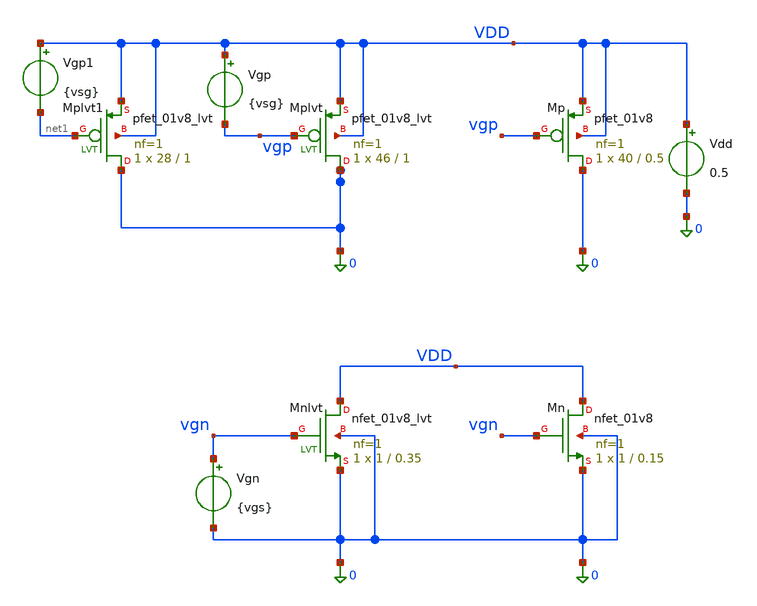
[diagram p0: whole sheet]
** sch_path: xschem/caracterizador.sch
**.subckt caracterizador
Vgp VDD vgp {vsg}
Vdd VDD 0 0.5
XMplvt 0 vgp VDD VDD sky130_fd_pr__pfet_01v8_lvt L=1 W=46 nf=1 ad='int((1 + 1)/2) * 46 / 1 * 0.29' as='int((1 + 2)/2) * 46 / 1 * 0.29'
+ pd='2*int((1 + 1)/2) * (46 / 1 + 0.29)' ps='2*int((1 + 2)/2) * (46 / 1 + 0.29)' nrd='0.29 / 46 ' nrs='0.29 / 46 '
+ sa=0 sb=0 sd=0 mult=1 m=1
XMp 0 vgp VDD VDD sky130_fd_pr__pfet_01v8 L=0.5 W=40 nf=1 ad='int((nf+1)/2) * W/nf * 0.29' as='int((nf+2)/2) * W/nf * 0.29'
+ pd='2*int((nf+1)/2) * (W/nf + 0.29)' ps='2*int((nf+2)/2) * (W/nf + 0.29)' nrd='0.29 / W' nrs='0.29 / W'
+ sa=0 sb=0 sd=0 mult=1 m=1
XMnlvt VDD vgn 0 0 sky130_fd_pr__nfet_01v8_lvt L=0.35 W=1 nf=1 ad='int((1 + 1)/2) * 1 / 1 * 0.29' as='int((1 + 2)/2) * 1 / 1 * 0.29'
+ pd='2*int((1 + 1)/2) * (1 / 1 + 0.29)' ps='2*int((1 + 2)/2) * (1 / 1 + 0.29)' nrd='0.29 / 1 ' nrs='0.29 / 1 '
+ sa=0 sb=0 sd=0 mult=1 m=1
XMn VDD vgn 0 0 sky130_fd_pr__nfet_01v8 L=0.15 W=1 nf=1 ad='int((1 + 1)/2) * 1 / 1 * 0.29' as='int((1 + 2)/2) * 1 / 1 * 0.29'
+ pd='2*int((1 + 1)/2) * (1 / 1 + 0.29)' ps='2*int((1 + 2)/2) * (1 / 1 + 0.29)' nrd='0.29 / 1 ' nrs='0.29 / 1 '
+ sa=0 sb=0 sd=0 mult=1 m=1
Vgn vgn 0 {vgs}
XMplvt1 0 net1 VDD VDD sky130_fd_pr__pfet_01v8_lvt L=1 W=28 nf=1 ad='int((1 + 1)/2) * 28 / 1 * 0.29'
+ as='int((1 + 2)/2) * 28 / 1 * 0.29' pd='2*int((1 + 1)/2) * (28 / 1 + 0.29)' ps='2*int((1 + 2)/2) * (28 / 1 + 0.29)'
+ nrd='0.29 / 28 ' nrs='0.29 / 28 ' sa=0 sb=0 sd=0 mult=1 m=1
Vgp1 VDD net1 {vsg}
**** begin user architecture code


* ==============================================================================
* Encabezado: Caracterizador Completo para PMOS y NMOS Sky130 (Std y LVT)
* Descripcion: Control de simulacion para extraer gm, ro, Id, Vth, Vdsat, Vov,
*              Cgg, ft y gm/Id de los 4 transistores (Mplvt, Mp, Mnlvt, Mn).
* ==============================================================================



* 1. Inclusión de libreria de modelos Sky130 PRIMERO
.lib /foss/pdks/sky130A/libs.tech/ngspice/sky130.lib.spice tt

.option temp=27


* Parametros de tension de polarizacion iniciales
.param vsg = 0.7
.param vgs = 0.6

* Parametros de dimensiones geometricas (en micrometros um)
.param wplvt = 1
.param lplvt = 0.35

.param wp = 1
.param lp = 0.15

.param wnlvt = 1
.param lnlvt = 0.35

.param wn = 1
.param ln = 0.15

.control
  * Forzar comportamiento estandar de SPICE para evitar errores numparam en Sky130
  set ngbehavior=ps

  save all

  * --- 1. GUARDAR PARAMETROS PMOS LVT (xMplvt) ---
  save @m.xMplvt.msky130_fd_pr__pfet_01v8_lvt[gm]
  save @m.xMplvt.msky130_fd_pr__pfet_01v8_lvt[gds]
  save @m.xMplvt.msky130_fd_pr__pfet_01v8_lvt[id]
  save @m.xMplvt.msky130_fd_pr__pfet_01v8_lvt[vth]
  save @m.xMplvt.msky130_fd_pr__pfet_01v8_lvt[vdsat]
  save @m.xMplvt.msky130_fd_pr__pfet_01v8_lvt[cgg]
  save @m.xMplvt.msky130_fd_pr__pfet_01v8_lvt[vgs]

  save @m.xMplvt1.msky130_fd_pr__pfet_01v8_lvt[gm]
  save @m.xMplvt1.msky130_fd_pr__pfet_01v8_lvt[gds]
  save @m.xMplvt1.msky130_fd_pr__pfet_01v8_lvt[id]
  save @m.xMplvt1.msky130_fd_pr__pfet_01v8_lvt[vth]
  save @m.xMplvt1.msky130_fd_pr__pfet_01v8_lvt[vdsat]
  save @m.xMplvt1.msky130_fd_pr__pfet_01v8_lvt[cgg]
  save @m.xMplvt1.msky130_fd_pr__pfet_01v8_lvt[vgs]

  * --- 2. GUARDAR PARAMETROS PMOS ESTANDAR (xMp) ---
  save @m.xMp.msky130_fd_pr__pfet_01v8[gm]
  save @m.xMp.msky130_fd_pr__pfet_01v8[gds]
  save @m.xMp.msky130_fd_pr__pfet_01v8[id]
  save @m.xMp.msky130_fd_pr__pfet_01v8[vth]
  save @m.xMp.msky130_fd_pr__pfet_01v8[vdsat]
  save @m.xMp.msky130_fd_pr__pfet_01v8[cgg]
  save @m.xMp.msky130_fd_pr__pfet_01v8[vgs]

  * --- 3. GUARDAR PARAMETROS NMOS LVT (xMnlvt) ---
  save @m.xMnlvt.msky130_fd_pr__nfet_01v8_lvt[gm]
  save @m.xMnlvt.msky130_fd_pr__nfet_01v8_lvt[gds]
  save @m.xMnlvt.msky130_fd_pr__nfet_01v8_lvt[id]
  save @m.xMnlvt.msky130_fd_pr__nfet_01v8_lvt[vth]
  save @m.xMnlvt.msky130_fd_pr__nfet_01v8_lvt[vdsat]
  save @m.xMnlvt.msky130_fd_pr__nfet_01v8_lvt[cgg]
  save @m.xMnlvt.msky130_fd_pr__nfet_01v8_lvt[vgs]

  * --- 4. GUARDAR PARAMETROS NMOS ESTANDAR (xMn) ---
  save @m.xMn.msky130_fd_pr__nfet_01v8[gm]
  save @m.xMn.msky130_fd_pr__nfet_01v8[gds]
  save @m.xMn.msky130_fd_pr__nfet_01v8[id]
  save @m.xMn.msky130_fd_pr__nfet_01v8[vth]
  save @m.xMn.msky130_fd_pr__nfet_01v8[vdsat]
  save @m.xMn.msky130_fd_pr__nfet_01v8[cgg]
  save @m.xMn.msky130_fd_pr__nfet_01v8[vgs]

  * Barrido DC de fuentes de voltaje Vgp (PMOS) y Vgn (NMOS) de 0V a 1.8V
  dc Vgp 0 1.8 0.01 Vgn 0 1.8 0.01

  * --- CALCULOS PMOS LVT (Mplvt) ---
  let ro_mplvt = 1 / @m.xMplvt.msky130_fd_pr__pfet_01v8_lvt[gds]
  let gm_id_mplvt = @m.xMplvt.msky130_fd_pr__pfet_01v8_lvt[gm] /
+ @m.xMplvt.msky130_fd_pr__pfet_01v8_lvt[id]
  let ft_mplvt = @m.xMplvt.msky130_fd_pr__pfet_01v8_lvt[gm] / (2 * pi *
+ @m.xMplvt.msky130_fd_pr__pfet_01v8_lvt[cgg])
  let vov_mplvt = abs(@m.xMplvt.msky130_fd_pr__pfet_01v8_lvt[vgs]) -
+ abs(@m.xMplvt.msky130_fd_pr__pfet_01v8_lvt[vth])

  * --- CALCULOS PMOS STD (Mp) ---
  let ro_mp = 1 / @m.xMp.msky130_fd_pr__pfet_01v8[gds]
  let gm_id_mp = @m.xMp.msky130_fd_pr__pfet_01v8[gm] / @m.xMp.msky130_fd_pr__pfet_01v8[id]
  let ft_mp = @m.xMp.msky130_fd_pr__pfet_01v8[gm] / (2 * pi * @m.xMp.msky130_fd_pr__pfet_01v8[cgg])
  let vov_mp = abs(@m.xMp.msky130_fd_pr__pfet_01v8[vgs]) - abs(@m.xMp.msky130_fd_pr__pfet_01v8[vth])

  * --- CALCULOS NMOS LVT (Mnlvt) ---
  let ro_mnlvt = 1 / @m.xMnlvt.msky130_fd_pr__nfet_01v8_lvt[gds]
  let gm_id_mnlvt = @m.xMnlvt.msky130_fd_pr__nfet_01v8_lvt[gm] /
+ @m.xMnlvt.msky130_fd_pr__nfet_01v8_lvt[id]
  let ft_mnlvt = @m.xMnlvt.msky130_fd_pr__nfet_01v8_lvt[gm] / (2 * pi *
+ @m.xMnlvt.msky130_fd_pr__nfet_01v8_lvt[cgg])
  let vov_mnlvt = @m.xMnlvt.msky130_fd_pr__nfet_01v8_lvt[vgs] -
+ @m.xMnlvt.msky130_fd_pr__nfet_01v8_lvt[vth]

  * --- CALCULOS NMOS STD (Mn) ---
  let ro_mn = 1 / @m.xMn.msky130_fd_pr__nfet_01v8[gds]
  let gm_id_mn = @m.xMn.msky130_fd_pr__nfet_01v8[gm] / @m.xMn.msky130_fd_pr__nfet_01v8[id]
  let ft_mn = @m.xMn.msky130_fd_pr__nfet_01v8[gm] / (2 * pi * @m.xMn.msky130_fd_pr__nfet_01v8[cgg])
  let vov_mn = @m.xMn.msky130_fd_pr__nfet_01v8[vgs] - @m.xMn.msky130_fd_pr__nfet_01v8[vth]

  * Guardar los resultados en archivo caracterizador.raw
  set filetype=ascii
  write caracterizador.raw all
op
write caracterizador_op.raw
plot vsense#branch
.endc



**** end user architecture code
**.ends
.end
